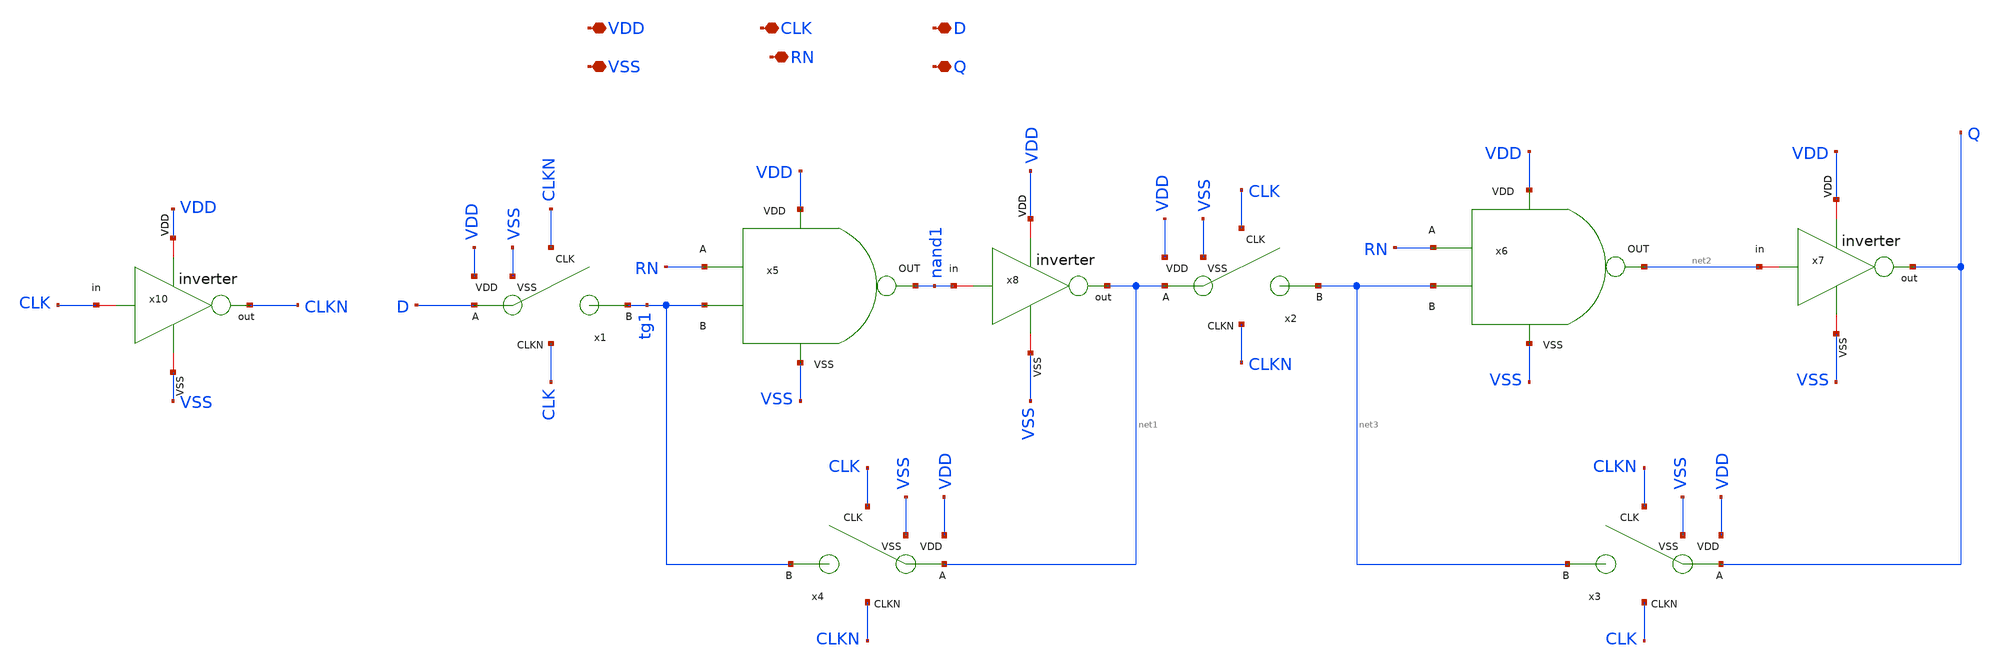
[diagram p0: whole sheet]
** sch_path: designs/sar_adc/digital/flip_flop/xschem/FF_D.sch
**.subckt FF_D VDD VSS CLK D RN Q
*.iopin VDD
*.iopin VSS
*.iopin CLK
*.iopin D
*.iopin RN
*.iopin Q
x1 CLKN D VDD tg1 CLK VSS TG
x2 CLK net1 VDD net3 CLKN VSS TG
x3 CLKN Q VDD net3 CLK VSS TG
x4 CLK net1 VDD tg1 CLKN VSS TG
x5 VDD VSS RN tg1 nand1 NAND
x6 VDD VSS RN net3 net2 NAND
x8 VDD nand1 net1 VSS inverter
x7 VDD net2 Q VSS inverter
x10 VDD CLK CLKN VSS inverter
**.ends

* expanding   symbol:  designs/sar_adc/digital/TG/xschem/TG.sym # of pins=6
** sym_path: designs/sar_adc/digital/TG/xschem/TG.sym
** sch_path: designs/sar_adc/digital/TG/xschem/TG.sch
.subckt TG CLK A VDD B CLKN VSS
*.iopin VDD
*.iopin VSS
*.ipin CLK
*.ipin CLKN
*.iopin A
*.iopin B
XM1 A CLK B VSS nfet_03v3 L=0.28u W=0.22u nf=1 ad='int((nf+1)/2) * W/nf * 0.18u' as='int((nf+2)/2) * W/nf * 0.18u'
+ pd='2*int((nf+1)/2) * (W/nf + 0.18u)' ps='2*int((nf+2)/2) * (W/nf + 0.18u)' nrd='0.18u / W' nrs='0.18u / W'
+ sa=0 sb=0 sd=0 m=1
XM2 A CLKN B VDD pfet_03v3 L=0.28u W=0.22u nf=1 ad='int((nf+1)/2) * W/nf * 0.18u' as='int((nf+2)/2) * W/nf * 0.18u'
+ pd='2*int((nf+1)/2) * (W/nf + 0.18u)' ps='2*int((nf+2)/2) * (W/nf + 0.18u)' nrd='0.18u / W' nrs='0.18u / W'
+ sa=0 sb=0 sd=0 m=1
.ends


* expanding   symbol:  designs/sar_adc/digital/NAND/xschem/NAND.sym # of pins=5
** sym_path: designs/sar_adc/digital/NAND/xschem/NAND.sym
** sch_path: designs/sar_adc/digital/NAND/xschem/NAND.sch
.subckt NAND VDD VSS A B out
*.iopin A
*.iopin B
*.iopin out
*.iopin VDD
*.iopin VSS
xINVA1 VDD net1 net2 VSS inverter
xINVB1[2] VDD net2 out VSS inverter
xINVB1[1] VDD net2 out VSS inverter
xINVB1[0] VDD net2 out VSS inverter
XM5 net1 A VDD VDD pfet_03v3 L=0.28u W=0.5u nf=1 ad='int((nf+1)/2) * W/nf * 0.18u' as='int((nf+2)/2) * W/nf * 0.18u'
+ pd='2*int((nf+1)/2) * (W/nf + 0.18u)' ps='2*int((nf+2)/2) * (W/nf + 0.18u)' nrd='0.18u / W' nrs='0.18u / W'
+ sa=0 sb=0 sd=0 m=2
XM6 net1 A net3 VSS nfet_03v3 L=0.28u W=0.5u nf=1 ad='int((nf+1)/2) * W/nf * 0.18u' as='int((nf+2)/2) * W/nf * 0.18u'
+ pd='2*int((nf+1)/2) * (W/nf + 0.18u)' ps='2*int((nf+2)/2) * (W/nf + 0.18u)' nrd='0.18u / W' nrs='0.18u / W'
+ sa=0 sb=0 sd=0 m=1
XM7 net1 B VDD VDD pfet_03v3 L=0.28u W=0.5u nf=1 ad='int((nf+1)/2) * W/nf * 0.18u' as='int((nf+2)/2) * W/nf * 0.18u'
+ pd='2*int((nf+1)/2) * (W/nf + 0.18u)' ps='2*int((nf+2)/2) * (W/nf + 0.18u)' nrd='0.18u / W' nrs='0.18u / W'
+ sa=0 sb=0 sd=0 m=2
XM8 net3 B VSS VSS nfet_03v3 L=0.28u W=0.5u nf=1 ad='int((nf+1)/2) * W/nf * 0.18u' as='int((nf+2)/2) * W/nf * 0.18u'
+ pd='2*int((nf+1)/2) * (W/nf + 0.18u)' ps='2*int((nf+2)/2) * (W/nf + 0.18u)' nrd='0.18u / W' nrs='0.18u / W'
+ sa=0 sb=0 sd=0 m=1
.ends


* expanding   symbol:  designs/sar_adc/digital/inverter/xschem/inverter.sym # of pins=6
** sym_path: designs/sar_adc/digital/inverter/xschem/inverter.sym
** sch_path: designs/sar_adc/digital/inverter/xschem/inverter.sch
.subckt inverter VDD in out VSS
*.opin out
*.iopin in
*.iopin VDD
*.iopin VSS
XM1 out in VSS VSS nfet_03v3 L=0.28u W=1u nf=1 ad='int((nf+1)/2) * W/nf * 0.18u' as='int((nf+2)/2) * W/nf * 0.18u'
+ pd='2*int((nf+1)/2) * (W/nf + 0.18u)' ps='2*int((nf+2)/2) * (W/nf + 0.18u)' nrd='0.18u / W' nrs='0.18u / W'
+ sa=0 sb=0 sd=0 m=1
XM2 out in VDD VDD pfet_03v3 L=0.28u W=3u nf=1 ad='int((nf+1)/2) * W/nf * 0.18u' as='int((nf+2)/2) * W/nf * 0.18u'
+ pd='2*int((nf+1)/2) * (W/nf + 0.18u)' ps='2*int((nf+2)/2) * (W/nf + 0.18u)' nrd='0.18u / W' nrs='0.18u / W'
+ sa=0 sb=0 sd=0 m=1
.ends

.end
